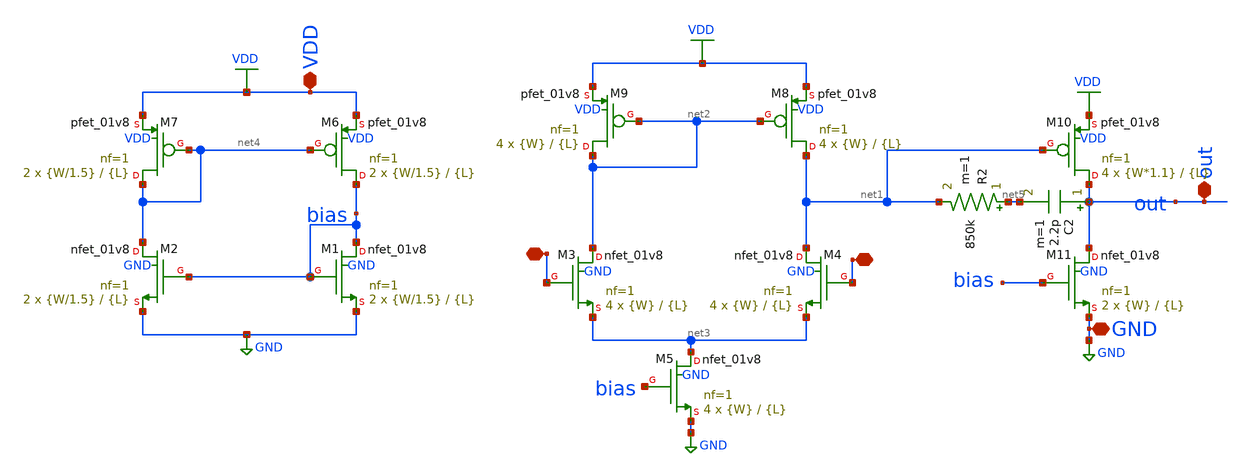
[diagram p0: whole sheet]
** sch_path: xschem/op1.sch
**.subckt op1 VDD GND - + out
*.iopin VDD
*.iopin GND
*.iopin -
*.iopin +
*.iopin out
C2 out net5 2.2p m=1
R2 net5 net1 850k m=1
XM1 bias bias GND GND sky130_fd_pr__nfet_01v8 L={L} W={W/1.5} nf=1 ad='int((nf+1)/2) * W/nf * 0.29' as='int((nf+2)/2) * W/nf * 0.29'
+ pd='2*int((nf+1)/2) * (W/nf + 0.29)' ps='2*int((nf+2)/2) * (W/nf + 0.29)' nrd='0.29 / W' nrs='0.29 / W'
+ sa=0 sb=0 sd=0 mult=2 m=2
XM2 net4 bias GND GND sky130_fd_pr__nfet_01v8 L={L} W={W/1.5} nf=1 ad='int((nf+1)/2) * W/nf * 0.29' as='int((nf+2)/2) * W/nf * 0.29'
+ pd='2*int((nf+1)/2) * (W/nf + 0.29)' ps='2*int((nf+2)/2) * (W/nf + 0.29)' nrd='0.29 / W' nrs='0.29 / W'
+ sa=0 sb=0 sd=0 mult=2 m=2
XM3 net2 - net3 GND sky130_fd_pr__nfet_01v8 L={L} W={W} nf=1 ad='int((nf+1)/2) * W/nf * 0.29' as='int((nf+2)/2) * W/nf * 0.29'
+ pd='2*int((nf+1)/2) * (W/nf + 0.29)' ps='2*int((nf+2)/2) * (W/nf + 0.29)' nrd='0.29 / W' nrs='0.29 / W'
+ sa=0 sb=0 sd=0 mult=4 m=4
XM4 net1 + net3 GND sky130_fd_pr__nfet_01v8 L={L} W={W} nf=1 ad='int((nf+1)/2) * W/nf * 0.29' as='int((nf+2)/2) * W/nf * 0.29'
+ pd='2*int((nf+1)/2) * (W/nf + 0.29)' ps='2*int((nf+2)/2) * (W/nf + 0.29)' nrd='0.29 / W' nrs='0.29 / W'
+ sa=0 sb=0 sd=0 mult=4 m=4
XM6 bias net4 VDD VDD sky130_fd_pr__pfet_01v8 L={L} W={W/1.5} nf=1 ad='int((nf+1)/2) * W/nf * 0.29' as='int((nf+2)/2) * W/nf * 0.29'
+ pd='2*int((nf+1)/2) * (W/nf + 0.29)' ps='2*int((nf+2)/2) * (W/nf + 0.29)' nrd='0.29 / W' nrs='0.29 / W'
+ sa=0 sb=0 sd=0 mult=2 m=2
XM7 net4 net4 VDD VDD sky130_fd_pr__pfet_01v8 L={L} W={W/1.5} nf=1 ad='int((nf+1)/2) * W/nf * 0.29' as='int((nf+2)/2) * W/nf * 0.29'
+ pd='2*int((nf+1)/2) * (W/nf + 0.29)' ps='2*int((nf+2)/2) * (W/nf + 0.29)' nrd='0.29 / W' nrs='0.29 / W'
+ sa=0 sb=0 sd=0 mult=2 m=2
XM8 net1 net2 VDD VDD sky130_fd_pr__pfet_01v8 L={L} W={W} nf=1 ad='int((nf+1)/2) * W/nf * 0.29' as='int((nf+2)/2) * W/nf * 0.29'
+ pd='2*int((nf+1)/2) * (W/nf + 0.29)' ps='2*int((nf+2)/2) * (W/nf + 0.29)' nrd='0.29 / W' nrs='0.29 / W'
+ sa=0 sb=0 sd=0 mult=4 m=4
XM9 net2 net2 VDD VDD sky130_fd_pr__pfet_01v8 L={L} W={W} nf=1 ad='int((nf+1)/2) * W/nf * 0.29' as='int((nf+2)/2) * W/nf * 0.29'
+ pd='2*int((nf+1)/2) * (W/nf + 0.29)' ps='2*int((nf+2)/2) * (W/nf + 0.29)' nrd='0.29 / W' nrs='0.29 / W'
+ sa=0 sb=0 sd=0 mult=4 m=4
XM5 net3 bias GND GND sky130_fd_pr__nfet_01v8 L={L} W={W} nf=1 ad='int((nf+1)/2) * W/nf * 0.29' as='int((nf+2)/2) * W/nf * 0.29'
+ pd='2*int((nf+1)/2) * (W/nf + 0.29)' ps='2*int((nf+2)/2) * (W/nf + 0.29)' nrd='0.29 / W' nrs='0.29 / W'
+ sa=0 sb=0 sd=0 mult=4 m=4
XM10 out net1 VDD VDD sky130_fd_pr__pfet_01v8 L={L} W={W*1.1} nf=1 ad='int((nf+1)/2) * W/nf * 0.29' as='int((nf+2)/2) * W/nf * 0.29'
+ pd='2*int((nf+1)/2) * (W/nf + 0.29)' ps='2*int((nf+2)/2) * (W/nf + 0.29)' nrd='0.29 / W' nrs='0.29 / W'
+ sa=0 sb=0 sd=0 mult=4 m=4
XM11 out bias GND GND sky130_fd_pr__nfet_01v8 L={L} W={W} nf=1 ad='int((nf+1)/2) * W/nf * 0.29' as='int((nf+2)/2) * W/nf * 0.29'
+ pd='2*int((nf+1)/2) * (W/nf + 0.29)' ps='2*int((nf+2)/2) * (W/nf + 0.29)' nrd='0.29 / W' nrs='0.29 / W'
+ sa=0 sb=0 sd=0 mult=2 m=2
**** begin user architecture code


.param L=20
.param W=1


**** end user architecture code
**.ends
.GLOBAL VDD
.GLOBAL GND
.end
